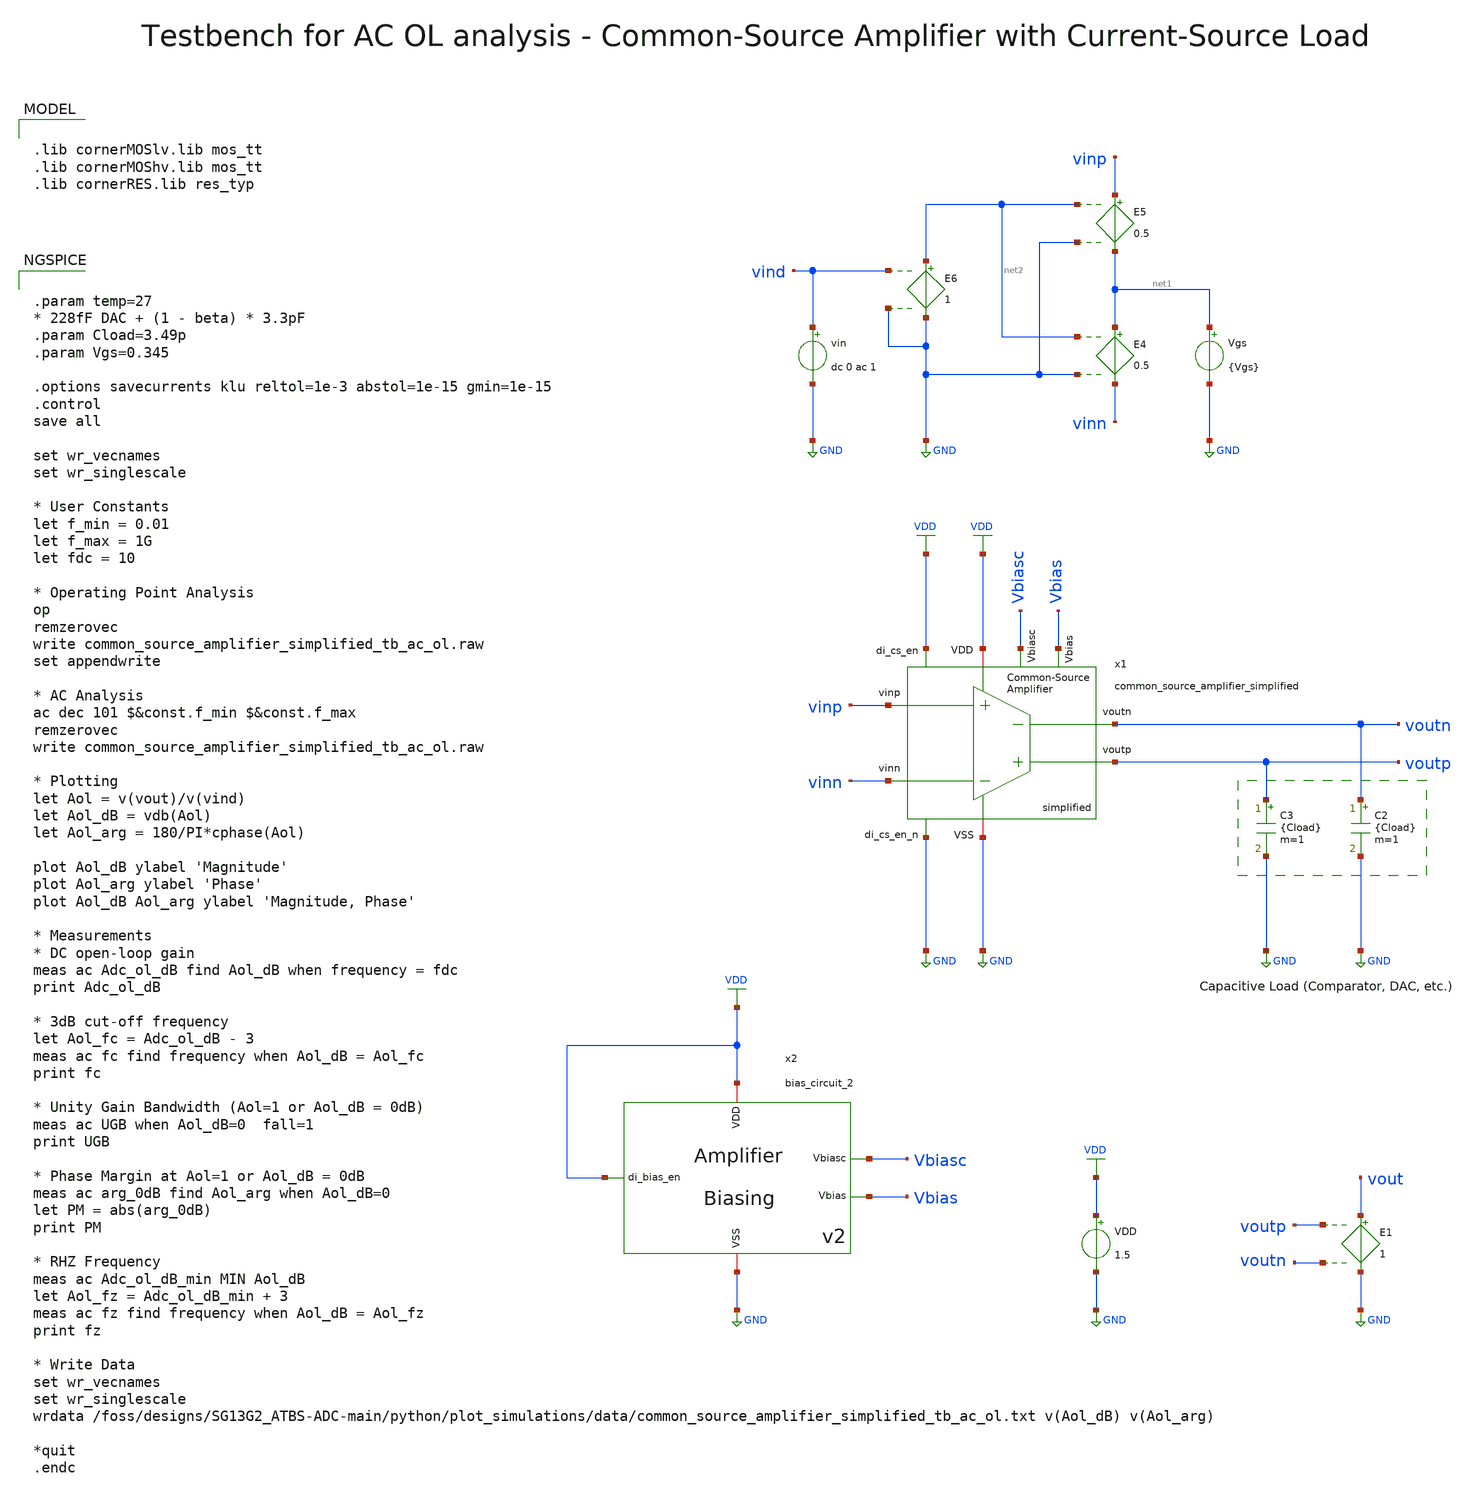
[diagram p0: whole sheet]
** sch_path: SG13G2_ATBS-ADC-main/xschem/bio_amplifier/amplifier_core/common_source_amplifier/testbenches/common_source_amplifier_simplified_tb_ac_ol.sch
**.subckt common_source_amplifier_simplified_tb_ac_ol
VDD VDD GND 1.5
Vgs net1 GND {Vgs}
E4 net1 vinn net2 GND 0.5
E5 vinp net1 net2 GND 0.5
E6 net2 GND vind GND 1
vin vind GND dc 0 ac 1
C2 voutn GND {Cload} m=1
C3 voutp GND {Cload} m=1
E1 vout GND voutp voutn 1
x1 VDD voutp voutn vinn vinp GND VDD GND Vbiasc Vbias common_source_amplifier_simplified
x2 VDD Vbiasc VDD GND Vbias bias_circuit_2
**** begin user architecture code


.param temp=27
* 228fF DAC + (1 - beta) * 3.3pF
.param Cload=3.49p
.param Vgs=0.345

.options savecurrents klu reltol=1e-3 abstol=1e-15 gmin=1e-15
.control
save all

set wr_vecnames
set wr_singlescale

* User Constants
let f_min = 0.01
let f_max = 1G
let fdc = 10

* Operating Point Analysis
op
remzerovec
write common_source_amplifier_simplified_tb_ac_ol.raw
set appendwrite

* AC Analysis
ac dec 101 $&const.f_min $&const.f_max
remzerovec
write common_source_amplifier_simplified_tb_ac_ol.raw

* Plotting
let Aol = v(vout)/v(vind)
let Aol_dB = vdb(Aol)
let Aol_arg = 180/PI*cphase(Aol)

plot Aol_dB ylabel 'Magnitude'
plot Aol_arg ylabel 'Phase'
plot Aol_dB Aol_arg ylabel 'Magnitude, Phase'

* Measurements
* DC open-loop gain
meas ac Adc_ol_dB find Aol_dB when frequency = fdc
print Adc_ol_dB

* 3dB cut-off frequency
let Aol_fc = Adc_ol_dB - 3
meas ac fc find frequency when Aol_dB = Aol_fc
print fc

* Unity Gain Bandwidth (Aol=1 or Aol_dB = 0dB)
meas ac UGB when Aol_dB=0  fall=1
print UGB

* Phase Margin at Aol=1 or Aol_dB = 0dB
meas ac arg_0dB find Aol_arg when Aol_dB=0
let PM = abs(arg_0dB)
print PM

* RHZ Frequency
meas ac Adc_ol_dB_min MIN Aol_dB
let Aol_fz = Adc_ol_dB_min + 3
meas ac fz find frequency when Aol_dB = Aol_fz
print fz

* Write Data
set wr_vecnames
set wr_singlescale
wrdata
+ /foss/designs/SG13G2_ATBS-ADC-main/python/plot_simulations/data/common_source_amplifier_simplified_tb_ac_ol.txt v(Aol_dB) v(Aol_arg)

*quit
.endc



.lib cornerMOSlv.lib mos_tt
.lib cornerMOShv.lib mos_tt
.lib cornerRES.lib res_typ

**** end user architecture code
**.ends

* expanding   symbol:
*+  bio_amplifier/amplifier_core/common_source_amplifier/common_source_amplifier_simplified.sym # of pins=10
** sym_path: SG13G2_ATBS-ADC-main/xschem/bio_amplifier/amplifier_core/common_source_amplifier/common_source_amplifier_simplified.sym
** sch_path: SG13G2_ATBS-ADC-main/xschem/bio_amplifier/amplifier_core/common_source_amplifier/common_source_amplifier_simplified.sch
.subckt common_source_amplifier_simplified VDD voutp voutn vinn vinp VSS di_cs_en di_cs_en_n Vbiasc
+ Vbias
*.ipin vinp
*.ipin vinn
*.opin voutp
*.opin voutn
*.iopin VDD
*.iopin VSS
*.ipin di_cs_en
*.ipin di_cs_en_n
*.ipin Vbias
*.ipin Vbiasc
xM12 net1 Vb VDD VDD sg13g2_lv_pmos_stacked_x4 W_P=8.0u L_P=40.0u NG_P=16 M_P=1
xM10 voutn vinp VSS VSS sg13g2_lv_nmos_stacked_x4 W_N=2.0u L_N=40.0u NG_N=4 M_N=1
R1 Vb net1 25.5Meg m=1
C3 Vb net1 900f m=1
xM13 voutp Vb VDD VDD sg13g2_lv_pmos_stacked_x4 W_P=8.0u L_P=40.0u NG_P=16 M_P=1
xM11 voutp vinn VSS VSS sg13g2_lv_nmos_stacked_x4 W_N=2.0u L_N=40.0u NG_N=4 M_N=1
C4 voutp Vb 900f m=1
R2 voutp Vb 25.5Meg m=1
xM15 net2 Vb VDD VDD sg13g2_lv_pmos_stacked_x4 W_P=2.0u L_P=40.0u NG_P=4 M_P=1
Vmeas1 net1 voutn 0
.save i(vmeas1)
XMpd2 net2 di_cs_en_n Vb VDD sg13_hv_pmos w=1.0u l=0.5u ng=1 m=1 mm_ok=1
XMpd1 Vb di_cs_en VDD VDD sg13_hv_pmos w=1.0u l=0.5u ng=1 m=1 mm_ok=1
Vmeas3 net2 net3 0
.save i(vmeas3)
xM14c net3 Vbiasc VSS net4 sg13g2_lv_nmos_stacked_x2 W_N=11.5u L_N=20.0u NG_N=23 M_N=1
xM14 net4 Vbias VSS VSS sg13g2_lv_nmos_stacked_x2 W_N=11.5u L_N=20.0u NG_N=23 M_N=1
.ends


* expanding   symbol:  bio_amplifier/amplifier_core/bias_circuit/bias_circuit_2/bias_circuit_2.sym #
*+ of pins=5
** sym_path: SG13G2_ATBS-ADC-main/xschem/bio_amplifier/amplifier_core/bias_circuit/bias_circuit_2/bias_circuit_2.sym
** sch_path: SG13G2_ATBS-ADC-main/xschem/bio_amplifier/amplifier_core/bias_circuit/bias_circuit_2/bias_circuit_2.sch
.subckt bias_circuit_2 di_bias_en Vbiasc VDD VSS Vbias
*.iopin VDD
*.iopin VSS
*.opin Vbias
*.ipin di_bias_en
*.opin Vbiasc
R1 net3 VSS 3.72Meg m=1
XMDEC1 net1 Vbias net1 net1 sg13_lv_nmos w=100.0u l=40.0u ng=100 m=1 mm_ok=1
VIref net4 net8 0
.save i(viref)
VIout net9 Vbiasc 0
.save i(viout)
x1 VDD di_bias_en bias_en_n VSS inverter_lv W_P=1.0u L_P=0.13u W_N=1.0u L_N=0.13u
xMSU2 Vsu net6 VSS VSS sg13g2_lv_nmos_stacked_x4 W_N=1.0u L_N=40.0u NG_N=1 M_N=1
xMSU1 net5 Vsu VSS net6 sg13g2_lv_nmos_stacked_x4 W_N=1.0u L_N=40.0u NG_N=1 M_N=1
Vmeas1 net4 net5 0
.save i(vmeas1)
Vmeas2 Vbias net6 0
.save i(vmeas2)
XMPD1 Vgs_m34 di_bias_en net2 net2 sg13_lv_pmos w=1.0u l=0.13u ng=1 m=1 mm_ok=1
XMPD2 net4 bias_en_n Vgs_m34 net2 sg13_lv_pmos w=1.0u l=0.13u ng=1 m=1 mm_ok=1
XMPD3 Vbias bias_en_n VSS VSS sg13_lv_nmos w=1.0u l=0.13u ng=1 m=1 mm_ok=1
VIref5 net1 VSS 0
.save i(viref5)
VIdd VDD net2 0
.save i(vidd)
CSU1 net10 Vsu 35f m=1
xM1 net7 Vbias VSS net3 sg13g2_lv_nmos_stacked_x2 W_N=20.0u L_N=20.0u NG_N=20 M_N=1
xM1c net8 Vbiasc VSS net7 sg13g2_lv_nmos_stacked_x2 W_N=5.0u L_N=20.0u NG_N=5 M_N=1
xM2 Vbias Vbias VSS VSS sg13g2_lv_nmos_stacked_x2 W_N=5.0u L_N=20.0u NG_N=5 M_N=1
xM2c Vbiasc Vbiasc VSS Vbias sg13g2_lv_nmos_stacked_x2 W_N=5.0u L_N=20.0u NG_N=5 M_N=1
XMDEC2 net2 Vgs_m34 net2 net2 sg13_lv_pmos w=25.0u l=40.0u ng=25 m=1 mm_ok=1
xM3 net4 Vgs_m34 net2 net2 sg13g2_lv_pmos_stacked_x4 W_P=20.0u L_P=40.0u NG_P=20 M_P=1
xM4 net9 Vgs_m34 net2 net2 sg13g2_lv_pmos_stacked_x4 W_P=20.0u L_P=40.0u NG_P=20 M_P=1
XMPD6 Vsu di_bias_en net10 net10 sg13_lv_pmos w=1.0u l=0.13u ng=1 m=1 mm_ok=1
XMPD4 Vbiasc bias_en_n VSS VSS sg13_lv_nmos w=1.0u l=0.13u ng=1 m=1 mm_ok=1
XMPD7 Vsu bias_en_n VSS VSS sg13_lv_nmos w=1.0u l=0.13u ng=1 m=1 mm_ok=1
XMPD5 net10 bias_en_n net2 net2 sg13_lv_pmos w=1.0u l=0.13u ng=1 m=1 mm_ok=1
.ends


* expanding   symbol:  stacked_transistors/sg13g2_lv_pmos_stacked/sg13g2_lv_pmos_stacked_x4.sym # of
*+ pins=4
** sym_path: SG13G2_ATBS-ADC-main/xschem/stacked_transistors/sg13g2_lv_pmos_stacked/sg13g2_lv_pmos_stacked_x4.sym
** sch_path: SG13G2_ATBS-ADC-main/xschem/stacked_transistors/sg13g2_lv_pmos_stacked/sg13g2_lv_pmos_stacked_x4.sch
.subckt sg13g2_lv_pmos_stacked_x4 D G B S  W_P=1.0u L_P=0.45u NG_P=1 M_P=1
*.iopin D
*.iopin S
*.iopin G
*.iopin B
XM1 net1 G S B sg13_lv_pmos w=W_P l=L_P/4 ng=NG_P m=M_P mm_ok=1
XM2 net3 G net1 B sg13_lv_pmos w=W_P l=L_P/4 ng=NG_P m=M_P mm_ok=1
XM3 net2 G net3 B sg13_lv_pmos w=W_P l=L_P/4 ng=NG_P m=M_P mm_ok=1
XM4 D G net2 B sg13_lv_pmos w=W_P l=L_P/4 ng=NG_P m=M_P mm_ok=1
.ends


* expanding   symbol:  stacked_transistors/sg13g2_lv_nmos_stacked/sg13g2_lv_nmos_stacked_x4.sym # of
*+ pins=4
** sym_path: SG13G2_ATBS-ADC-main/xschem/stacked_transistors/sg13g2_lv_nmos_stacked/sg13g2_lv_nmos_stacked_x4.sym
** sch_path: SG13G2_ATBS-ADC-main/xschem/stacked_transistors/sg13g2_lv_nmos_stacked/sg13g2_lv_nmos_stacked_x4.sch
.subckt sg13g2_lv_nmos_stacked_x4 D G B S  W_N=1.0u L_N=0.45u NG_N=1 M_N=1
*.iopin D
*.iopin S
*.iopin G
*.iopin B
XM1 net1 G S B sg13_lv_nmos w=W_N l=L_N/4 ng=NG_N m=M_N mm_ok=1
XM2 net3 G net1 B sg13_lv_nmos w=W_N l=L_N/4 ng=NG_N m=M_N mm_ok=1
XM3 net2 G net3 B sg13_lv_nmos w=W_N l=L_N/4 ng=NG_N m=M_N mm_ok=1
XM4 D G net2 B sg13_lv_nmos w=W_N l=L_N/4 ng=NG_N m=M_N mm_ok=1
.ends


* expanding   symbol:  stacked_transistors/sg13g2_lv_nmos_stacked/sg13g2_lv_nmos_stacked_x2.sym # of
*+ pins=4
** sym_path: SG13G2_ATBS-ADC-main/xschem/stacked_transistors/sg13g2_lv_nmos_stacked/sg13g2_lv_nmos_stacked_x2.sym
** sch_path: SG13G2_ATBS-ADC-main/xschem/stacked_transistors/sg13g2_lv_nmos_stacked/sg13g2_lv_nmos_stacked_x2.sch
.subckt sg13g2_lv_nmos_stacked_x2 D G B S  W_N=1.0u L_N=0.45u NG_N=1 M_N=1
*.iopin D
*.iopin S
*.iopin G
*.iopin B
XM1 net1 G S B sg13_lv_nmos w=W_N l=L_N/2 ng=NG_N m=M_N mm_ok=1
XM2 D G net1 B sg13_lv_nmos w=W_N l=L_N/2 ng=NG_N m=M_N mm_ok=1
.ends


* expanding   symbol:  inverter/inverter_lv.sym # of pins=4
** sym_path: SG13G2_ATBS-ADC-main/xschem/inverter/inverter_lv.sym
** sch_path: SG13G2_ATBS-ADC-main/xschem/inverter/inverter_lv.sch
.subckt inverter_lv VDD vin vout VSS  W_P=3.0u L_P=0.13u W_N=1.0u L_N=0.13u
*.ipin vin
*.iopin VDD
*.iopin VSS
*.opin vout
XM1 vout vin VDD VDD sg13_lv_pmos w=W_P l=L_P ng=1 m=1 mm_ok=1
XM2 vout vin VSS VSS sg13_lv_nmos w=W_N l=L_N ng=1 m=1 mm_ok=1
.ends

.GLOBAL GND
.GLOBAL VDD
.end
